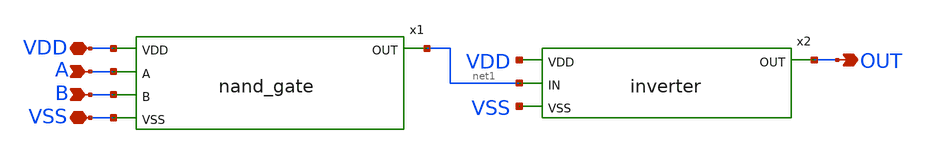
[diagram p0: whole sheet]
** sch_path: xschem/and_gate.sch
**.subckt and_gate VSS VDD A OUT B
*.iopin VSS
*.iopin VDD
*.ipin A
*.opin OUT
*.ipin B
x1 VDD A net1 B VSS nand_gate
x2 VDD net1 OUT VSS inverter
**.ends
.end
